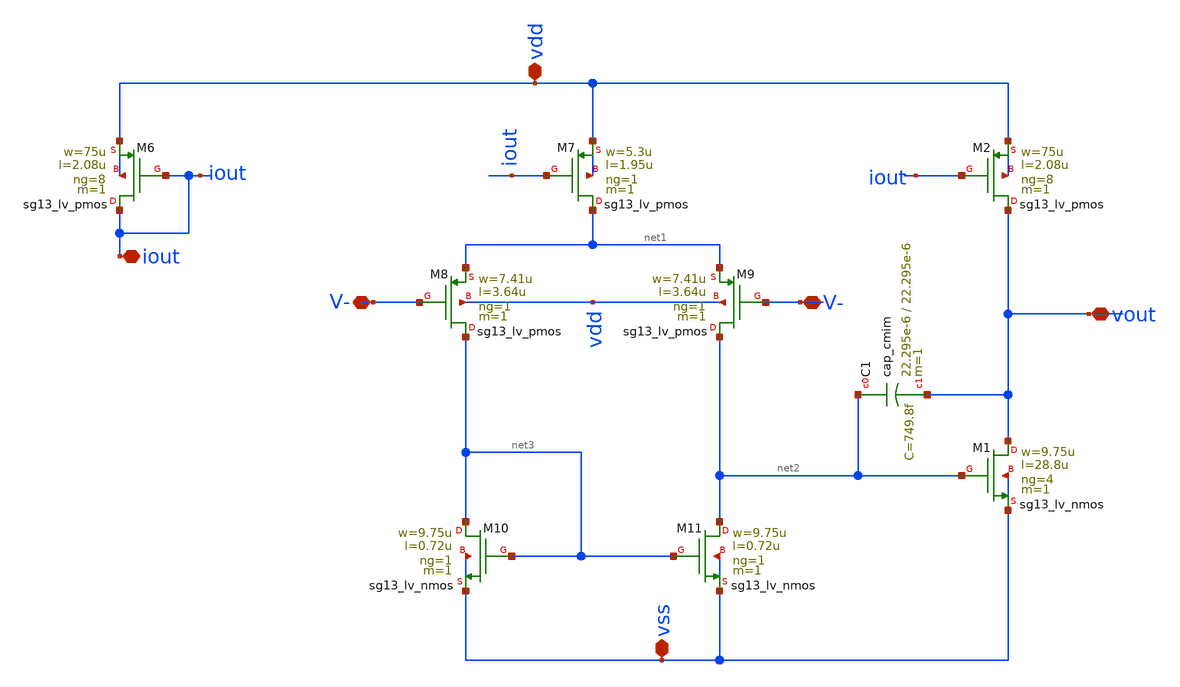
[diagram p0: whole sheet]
** sch_path: BTDay7-Ex/Ex1_Lecture7.sch
**.subckt Ex1_Lecture7 vdd iout V- vss V- vout
*.iopin vdd
*.iopin iout
*.iopin V-
*.iopin vss
*.iopin V-
*.iopin vout
XM6 iout iout vdd vdd sg13_lv_pmos w=75u l=2.08u ng=8 m=1 mm_ok=1
XM7 net1 iout vdd vdd sg13_lv_pmos w=5.3u l=1.95u ng=1 m=1 mm_ok=1
XM8 net3 V- net1 vdd sg13_lv_pmos w=7.41u l=3.64u ng=1 m=1 mm_ok=1
XM9 net2 V- net1 vdd sg13_lv_pmos w=7.41u l=3.64u ng=1 m=1 mm_ok=1
XM10 net3 net3 vss vss sg13_lv_nmos w=9.75u l=0.72u ng=1 m=1 mm_ok=1
XM11 net2 net3 vss vss sg13_lv_nmos w=9.75u l=0.72u ng=1 m=1 mm_ok=1
XM1 vout net2 vss vss sg13_lv_nmos w=9.75u l=28.8u ng=4 m=1 mm_ok=1
XM2 vout iout vdd vdd sg13_lv_pmos w=75u l=2.08u ng=8 m=1 mm_ok=1
XC1 net2 vout cap_cmim w=22.295e-6 l=22.295e-6 m=1 mm_ok=1
**.ends
.end
